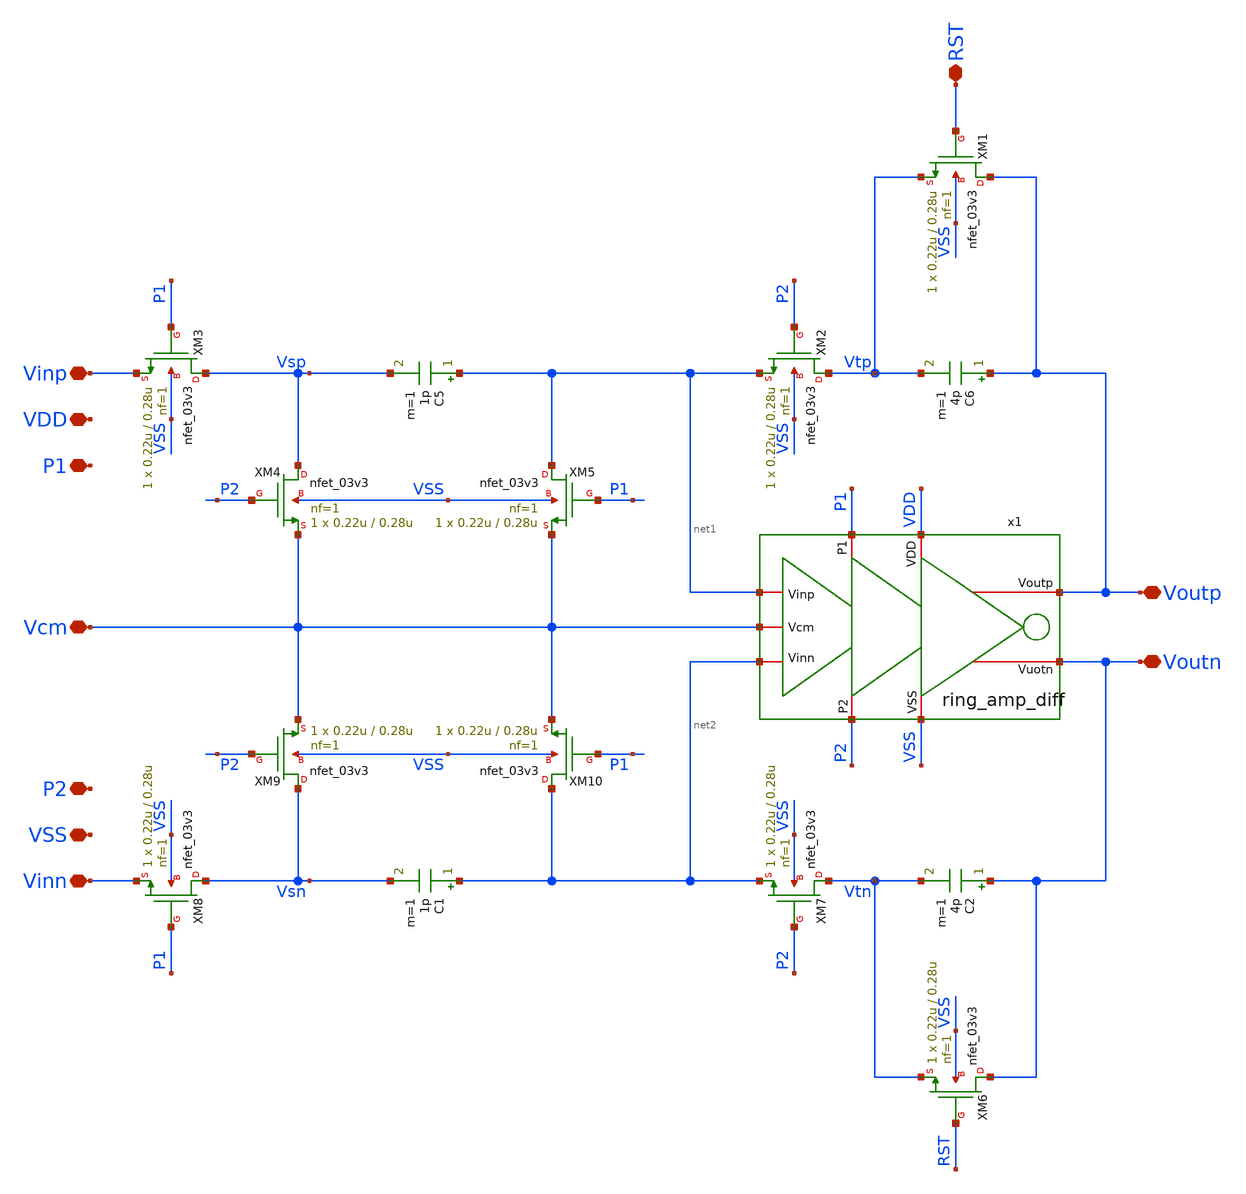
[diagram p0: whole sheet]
** sch_path: designs/DS_modulator/integrator/xschem/integrator.sch
**.subckt integrator Vinp Vcm Vinn Voutp Voutn RST VDD P1 VSS P2
*.iopin Vinp
*.iopin Vcm
*.iopin Vinn
*.iopin Voutp
*.iopin Voutn
*.iopin RST
*.iopin VDD
*.iopin P1
*.iopin VSS
*.iopin P2
x1 P1 P2 VDD VSS net1 Voutp Vcm Voutn net2 ring_amp_diff
XM1 Voutp RST Vtp VSS nfet_03v3 L=0.28u W=0.22u nf=1 ad='int((nf+1)/2) * W/nf * 0.18u' as='int((nf+2)/2) * W/nf * 0.18u'
+ pd='2*int((nf+1)/2) * (W/nf + 0.18u)' ps='2*int((nf+2)/2) * (W/nf + 0.18u)' nrd='0.18u / W' nrs='0.18u / W'
+ sa=0 sb=0 sd=0 m=1
XM2 Vtp P2 net1 VSS nfet_03v3 L=0.28u W=0.22u nf=1 ad='int((nf+1)/2) * W/nf * 0.18u' as='int((nf+2)/2) * W/nf * 0.18u'
+ pd='2*int((nf+1)/2) * (W/nf + 0.18u)' ps='2*int((nf+2)/2) * (W/nf + 0.18u)' nrd='0.18u / W' nrs='0.18u / W'
+ sa=0 sb=0 sd=0 m=1
XM3 Vsp P1 Vinp VSS nfet_03v3 L=0.28u W=0.22u nf=1 ad='int((nf+1)/2) * W/nf * 0.18u' as='int((nf+2)/2) * W/nf * 0.18u'
+ pd='2*int((nf+1)/2) * (W/nf + 0.18u)' ps='2*int((nf+2)/2) * (W/nf + 0.18u)' nrd='0.18u / W' nrs='0.18u / W'
+ sa=0 sb=0 sd=0 m=1
XM4 Vsp P2 Vcm VSS nfet_03v3 L=0.28u W=0.22u nf=1 ad='int((nf+1)/2) * W/nf * 0.18u' as='int((nf+2)/2) * W/nf * 0.18u'
+ pd='2*int((nf+1)/2) * (W/nf + 0.18u)' ps='2*int((nf+2)/2) * (W/nf + 0.18u)' nrd='0.18u / W' nrs='0.18u / W'
+ sa=0 sb=0 sd=0 m=1
XM5 net1 P1 Vcm VSS nfet_03v3 L=0.28u W=0.22u nf=1 ad='int((nf+1)/2) * W/nf * 0.18u' as='int((nf+2)/2) * W/nf * 0.18u'
+ pd='2*int((nf+1)/2) * (W/nf + 0.18u)' ps='2*int((nf+2)/2) * (W/nf + 0.18u)' nrd='0.18u / W' nrs='0.18u / W'
+ sa=0 sb=0 sd=0 m=1
XM6 Voutn RST Vtn VSS nfet_03v3 L=0.28u W=0.22u nf=1 ad='int((nf+1)/2) * W/nf * 0.18u' as='int((nf+2)/2) * W/nf * 0.18u'
+ pd='2*int((nf+1)/2) * (W/nf + 0.18u)' ps='2*int((nf+2)/2) * (W/nf + 0.18u)' nrd='0.18u / W' nrs='0.18u / W'
+ sa=0 sb=0 sd=0 m=1
XM7 Vtn P2 net2 VSS nfet_03v3 L=0.28u W=0.22u nf=1 ad='int((nf+1)/2) * W/nf * 0.18u' as='int((nf+2)/2) * W/nf * 0.18u'
+ pd='2*int((nf+1)/2) * (W/nf + 0.18u)' ps='2*int((nf+2)/2) * (W/nf + 0.18u)' nrd='0.18u / W' nrs='0.18u / W'
+ sa=0 sb=0 sd=0 m=1
XM8 Vsn P1 Vinn VSS nfet_03v3 L=0.28u W=0.22u nf=1 ad='int((nf+1)/2) * W/nf * 0.18u' as='int((nf+2)/2) * W/nf * 0.18u'
+ pd='2*int((nf+1)/2) * (W/nf + 0.18u)' ps='2*int((nf+2)/2) * (W/nf + 0.18u)' nrd='0.18u / W' nrs='0.18u / W'
+ sa=0 sb=0 sd=0 m=1
XM9 Vsn P2 Vcm VSS nfet_03v3 L=0.28u W=0.22u nf=1 ad='int((nf+1)/2) * W/nf * 0.18u' as='int((nf+2)/2) * W/nf * 0.18u'
+ pd='2*int((nf+1)/2) * (W/nf + 0.18u)' ps='2*int((nf+2)/2) * (W/nf + 0.18u)' nrd='0.18u / W' nrs='0.18u / W'
+ sa=0 sb=0 sd=0 m=1
XM10 net2 P1 Vcm VSS nfet_03v3 L=0.28u W=0.22u nf=1 ad='int((nf+1)/2) * W/nf * 0.18u' as='int((nf+2)/2) * W/nf * 0.18u'
+ pd='2*int((nf+1)/2) * (W/nf + 0.18u)' ps='2*int((nf+2)/2) * (W/nf + 0.18u)' nrd='0.18u / W' nrs='0.18u / W'
+ sa=0 sb=0 sd=0 m=1
C5 net1 Vsp 1p m=1
C6 Voutp Vtp 4p m=1
C1 net2 Vsn 1p m=1
C2 Voutn Vtn 4p m=1
**.ends
.end
